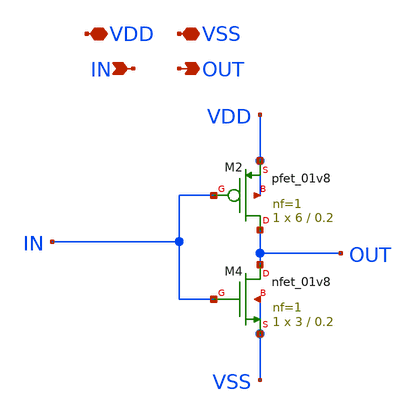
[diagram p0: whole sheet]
** sch_path: Xschem/PLL_TOP_Schematics/INV.sch
**.subckt INV VDD VSS IN OUT
*.iopin VDD
*.iopin VSS
*.ipin IN
*.opin OUT
XM2 OUT IN VDD VDD sky130_fd_pr__pfet_01v8 L=0.2 W=6 nf=1 ad='int((nf+1)/2) * W/nf * 0.29' as='int((nf+2)/2) * W/nf * 0.29'
+ pd='2*int((nf+1)/2) * (W/nf + 0.29)' ps='2*int((nf+2)/2) * (W/nf + 0.29)' nrd='0.29 / W' nrs='0.29 / W'
+ sa=0 sb=0 sd=0 mult=1 m=1
XM4 OUT IN VSS VSS sky130_fd_pr__nfet_01v8 L=0.2 W=3 nf=1 ad='int((nf+1)/2) * W/nf * 0.29' as='int((nf+2)/2) * W/nf * 0.29'
+ pd='2*int((nf+1)/2) * (W/nf + 0.29)' ps='2*int((nf+2)/2) * (W/nf + 0.29)' nrd='0.29 / W' nrs='0.29 / W'
+ sa=0 sb=0 sd=0 mult=1 m=1
**.ends
.end
